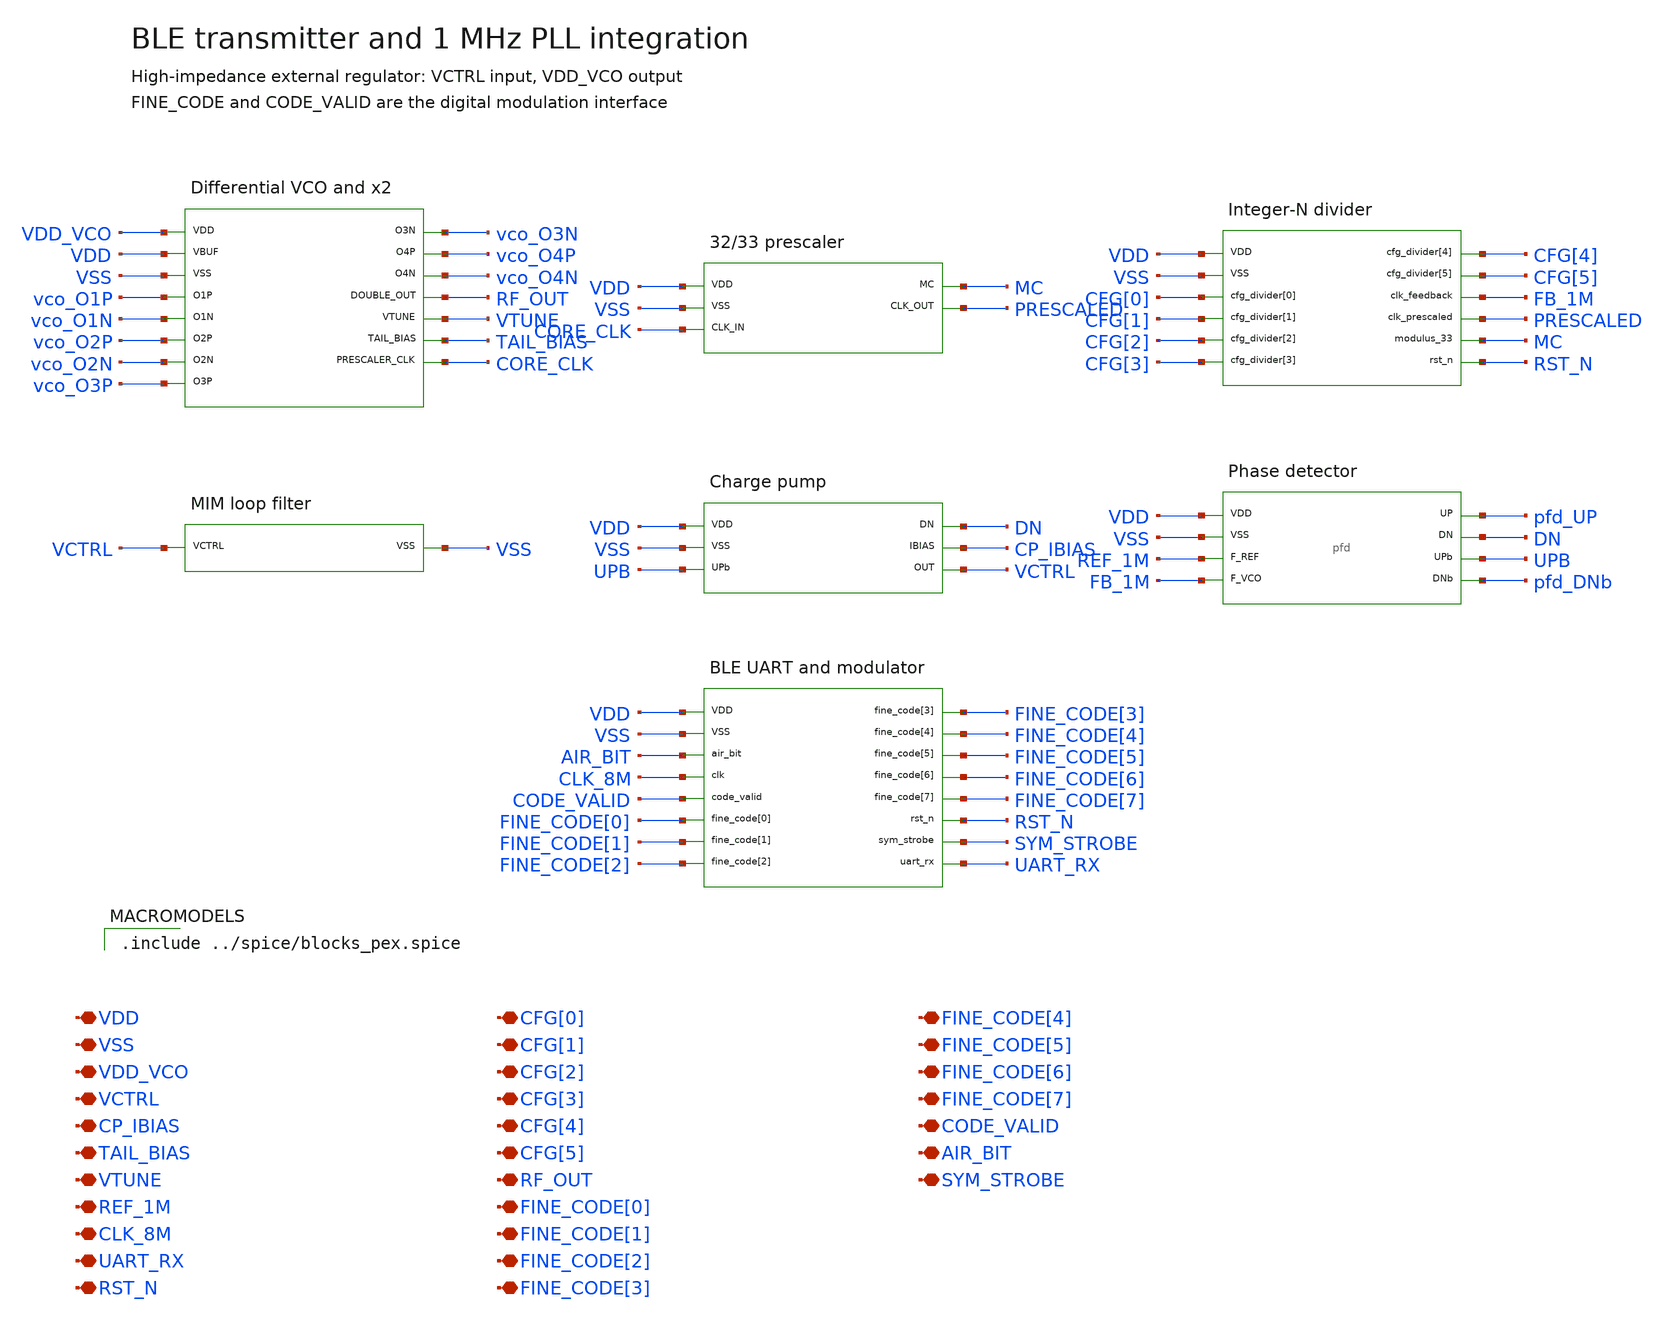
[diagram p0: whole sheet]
** sch_path: build/schematics/A01_topcell.sch
**.subckt A01_topcell VDD VSS VDD_VCO VCTRL CP_IBIAS TAIL_BIAS VTUNE REF_1M CLK_8M UART_RX RST_N
*+ CFG[0] CFG[1] CFG[2] CFG[3] CFG[4] CFG[5] RF_OUT FINE_CODE[0] FINE_CODE[1] FINE_CODE[2] FINE_CODE[3]
*+ FINE_CODE[4] FINE_CODE[5] FINE_CODE[6] FINE_CODE[7] CODE_VALID AIR_BIT SYM_STROBE
*.iopin VDD
*.iopin VSS
*.iopin VDD_VCO
*.iopin VCTRL
*.iopin CP_IBIAS
*.iopin TAIL_BIAS
*.iopin VTUNE
*.iopin REF_1M
*.iopin CLK_8M
*.iopin UART_RX
*.iopin RST_N
*.iopin CFG[0]
*.iopin CFG[1]
*.iopin CFG[2]
*.iopin CFG[3]
*.iopin CFG[4]
*.iopin CFG[5]
*.iopin RF_OUT
*.iopin FINE_CODE[0]
*.iopin FINE_CODE[1]
*.iopin FINE_CODE[2]
*.iopin FINE_CODE[3]
*.iopin FINE_CODE[4]
*.iopin FINE_CODE[5]
*.iopin FINE_CODE[6]
*.iopin FINE_CODE[7]
*.iopin CODE_VALID
*.iopin AIR_BIT
*.iopin SYM_STROBE
Xtx VDD VSS AIR_BIT CLK_8M CODE_VALID FINE_CODE[0] FINE_CODE[1] FINE_CODE[2] FINE_CODE[3]
+ FINE_CODE[4] FINE_CODE[5] FINE_CODE[6] FINE_CODE[7] RST_N SYM_STROBE UART_RX ble_tx_uart
Xdivider VDD VSS CFG[0] CFG[1] CFG[2] CFG[3] CFG[4] CFG[5] FB_1M PRESCALED MC RST_N
+ ble_feedback_divider
Xprescaler VDD VSS CORE_CLK MC PRESCALED x32_33_Prescaler_PEX
Xvco VDD_VCO VDD VSS vco_O1P vco_O1N vco_O2P vco_O2N vco_O3P vco_O3N vco_O4P vco_O4N RF_OUT VTUNE
+ TAIL_BIAS CORE_CLK VCO_PEX
Xpfd VDD VSS REF_1M FB_1M pfd_UP DN UPB pfd_DNb Phase_Detector_FE_PEX
Xpump VDD VSS UPB DN CP_IBIAS VCTRL Charge_Pump_FE_PEX
Xloop VCTRL VSS PLL_LOOP_FILTER
**** begin user architecture code

.include ../spice/blocks_pex.spice

**** end user architecture code
**.ends

* expanding   symbol:  tx.sym # of pins=16
** sym_path: build/schematics/tx.sym
* Definition in blocks_pex.spice

* expanding   symbol:  divider.sym # of pins=12
** sym_path: build/schematics/divider.sym
* Definition in blocks_pex.spice

* expanding   symbol:  prescaler.sym # of pins=5
** sym_path: build/schematics/prescaler.sym
* Definition in blocks_pex.spice

* expanding   symbol:  vco.sym # of pins=15
** sym_path: build/schematics/vco.sym
* Definition in blocks_pex.spice

* expanding   symbol:  pfd.sym # of pins=8
** sym_path: build/schematics/pfd.sym
* Definition in blocks_pex.spice

* expanding   symbol:  pump.sym # of pins=6
** sym_path: build/schematics/pump.sym
* Definition in blocks_pex.spice

* expanding   symbol:  loop.sym # of pins=2
** sym_path: build/schematics/loop.sym
* Definition in blocks_pex.spice
.end
